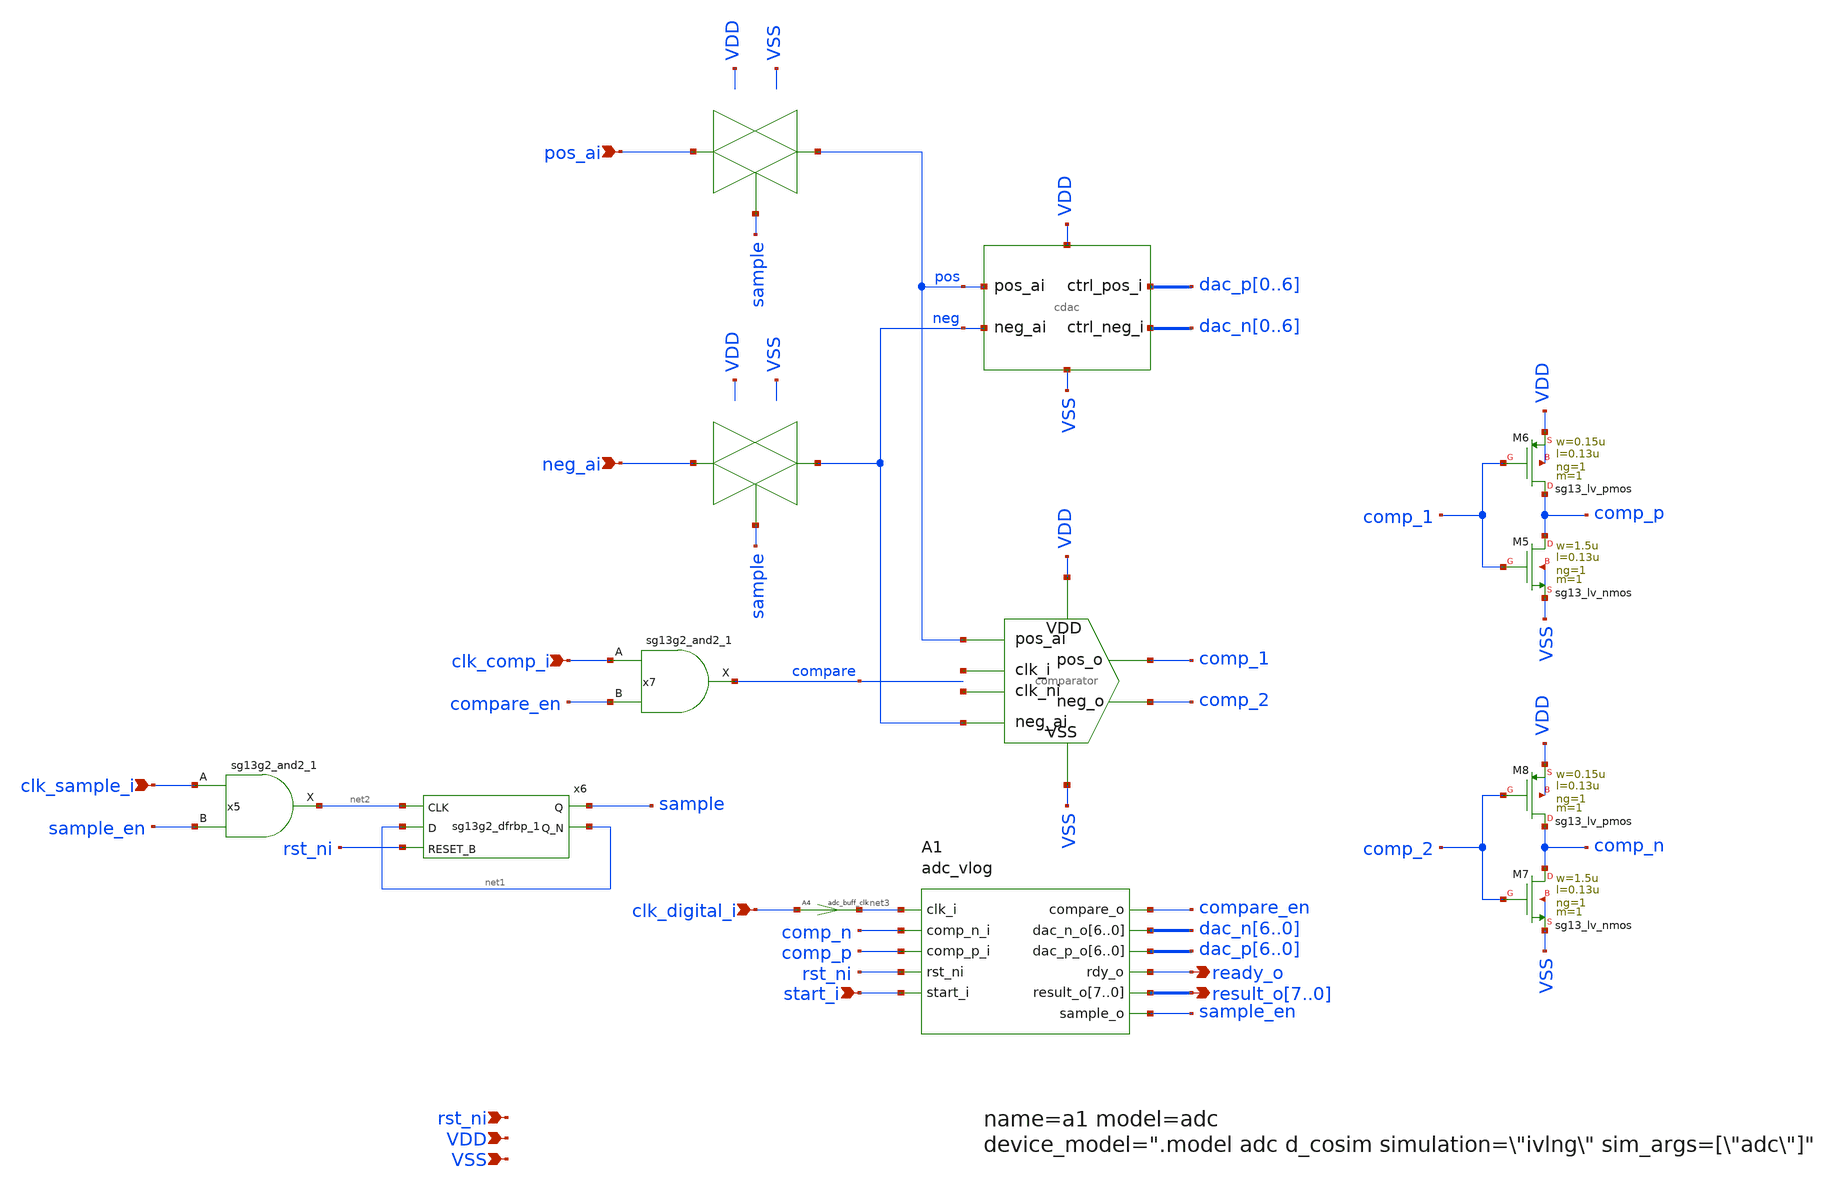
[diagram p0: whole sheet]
** sch_path: project/xschem_gatelevel/adc.sch
* IHP-GmbH/IHP-Open-PDK/ihp-sg13g2/libs.tech/xschem/sg13g2_stdcells/sg13g2_inv_2.sch:
* Copyright 2023 IHP PDK Authors
* Licensed under the Apache License, Version 2.0 (the "License");
**.subckt adc pos_ai VSS VDD clk_comp_i neg_ai clk_sample_i rst_ni clk_digital_i start_i ready_o
*+ result_o7,result_o6,result_o5,result_o4,result_o3,result_o2,result_o1,result_o0
*.ipin pos_ai
*.ipin VSS
*.ipin VDD
*.ipin clk_comp_i
*.ipin neg_ai
*.ipin clk_sample_i
*.ipin rst_ni
*.ipin clk_digital_i
*.ipin start_i
*.opin ready_o
*.opin result_o7,result_o6,result_o5,result_o4,result_o3,result_o2,result_o1,result_o0
x2 net4 pos neg comp_2 comp_1 VSS VDD net5 comparator
x4 pos neg VSS VDD dac_p0 dac_p1 dac_p2 dac_p3 dac_p4 dac_p5 dac_p6 dac_p0 dac_n0 dac_n1 dac_n2
+ dac_n3 dac_n4 dac_n5 dac_n6 dac_n0 cdac
XM5 comp_p comp_1 VSS VSS sg13_lv_nmos w=1.5u l=0.13u ng=1 m=1 mm_ok=1
XM6 comp_p comp_1 VDD VDD sg13_lv_pmos w=0.15u l=0.13u ng=1 m=1 mm_ok=1
XM7 comp_n comp_2 VSS VSS sg13_lv_nmos w=1.5u l=0.13u ng=1 m=1 mm_ok=1
XM8 comp_n comp_2 VDD VDD sg13_lv_pmos w=0.15u l=0.13u ng=1 m=1 mm_ok=1
x6 sample net1 net2 net1 rst_ni VDD VSS sg13g2_dfrbp_1
x5 net2 clk_sample_i sample_en VDD VSS sg13g2_and2_1
x7 compare clk_comp_i compare_en VDD VSS sg13g2_and2_1
A4 [ clk_digital_i ] [ net3 ] adc_buff_clk
A1 [ net3 comp_n comp_p rst_ni start_i ] [ compare_en dac_n6 dac_n5 dac_n4 dac_n3 dac_n2 dac_n1
+ dac_n0 dac_p6 dac_p5 dac_p4 dac_p3 dac_p2 dac_p1 dac_p0 ready_o result_o7 result_o6 result_o5 result_o4
+ result_o3 result_o2 result_o1 result_o0 sample_en ] adc
**.ends

* expanding   symbol:  ./comparator.sym # of pins=8
** sym_path: designs/comparator_dt/comparator.sym
** sch_path: designs/comparator_dt/comparator.sch
.subckt comparator clk_i pos_ai neg_ai neg_o pos_o VSS VDD clk_ni
*.ipin pos_ai
*.ipin neg_ai
*.ipin VSS
*.ipin VDD
*.opin neg_o
*.opin pos_o
*.ipin clk_i
*.ipin clk_ni
XM12 neg_buf clk_i VDD VDD sg13_lv_pmos w=1.0u l=0.13u ng=1 m=1 mm_ok=1
XM13 pos_buf clk_i VDD VDD sg13_lv_pmos w=1.0u l=0.13u ng=1 m=1 mm_ok=1
XM14 net1 pos_ai neg_buf VSS sg13_lv_nmos w=1.0u l=0.13u ng=1 m=1 mm_ok=1
XM15 net1 neg_ai pos_buf VSS sg13_lv_nmos w=1.0u l=0.13u ng=1 m=1 mm_ok=1
XM16 VSS clk_i net1 VSS sg13_lv_nmos w=1.0u l=0.13u ng=1 m=1 mm_ok=1
XM17 net2 clk_ni VDD VDD sg13_lv_pmos w=2.0u l=0.13u ng=2 m=1 mm_ok=1
XM18 pos_o neg_o net2 VDD sg13_lv_pmos w=2.0u l=0.13u ng=2 m=1 mm_ok=1
XM19 neg_o pos_o net2 VDD sg13_lv_pmos w=2.0u l=0.13u ng=2 m=1 mm_ok=1
XM20 VSS neg_buf pos_o VSS sg13_lv_nmos w=1.0u l=0.13u ng=1 m=1 mm_ok=1
XM21 VSS neg_o pos_o VSS sg13_lv_nmos w=1.0u l=0.13u ng=1 m=1 mm_ok=1
XM22 VSS pos_o neg_o VSS sg13_lv_nmos w=1.0u l=0.13u ng=1 m=1 mm_ok=1
XM23 VSS pos_buf neg_o VSS sg13_lv_nmos w=1.0u l=0.13u ng=1 m=1 mm_ok=1
XC1 neg_buf VSS cap_cmim w=1.41e-5 l=1.41e-5 m=1 mm_ok=1
XC2 pos_buf VSS cap_cmim w=1.41e-5 l=1.41e-5 m=1 mm_ok=1
.ends


* expanding   symbol:  ./cdac.sym # of pins=6
** sym_path: designs/cdac_diff/cdac.sym
** sch_path: designs/cdac_diff/cdac.sch
.subckt cdac pos_ai neg_ai VSS VDD pos_ctrl_i0 pos_ctrl_i1 pos_ctrl_i2 pos_ctrl_i3 pos_ctrl_i4
+ pos_ctrl_i5 pos_ctrl_i6 pos_ctrl_i7 neg_ctrl_i0 neg_ctrl_i1 neg_ctrl_i2 neg_ctrl_i3 neg_ctrl_i4 neg_ctrl_i5
+ neg_ctrl_i6 neg_ctrl_i7
*.ipin pos_ai
*.ipin VSS
*.ipin VDD
*.ipin neg_ai
*.ipin
*+ pos_ctrl_i0,pos_ctrl_i1,pos_ctrl_i2,pos_ctrl_i3,pos_ctrl_i4,pos_ctrl_i5,pos_ctrl_i6,pos_ctrl_i7
*.ipin
*+ neg_ctrl_i0,neg_ctrl_i1,neg_ctrl_i2,neg_ctrl_i3,neg_ctrl_i4,neg_ctrl_i5,neg_ctrl_i6,neg_ctrl_i7
x1 net1 pos_ctrl_i0 VDD VSS sg13g2_inv_2
x2 net2 pos_ctrl_i1 VDD VSS sg13g2_inv_2
x3 net3 pos_ctrl_i2 VDD VSS sg13g2_inv_2
x4 net4 pos_ctrl_i3 VDD VSS sg13g2_inv_2
x5 net5 pos_ctrl_i4 VDD VSS sg13g2_inv_2
x6 net6 pos_ctrl_i5 VDD VSS sg13g2_inv_2
x7 net7 pos_ctrl_i6 VDD VSS sg13g2_inv_2
x8 net8 pos_ctrl_i7 VDD VSS sg13g2_inv_2
XC1 pos_ai net8 cap_cmim w=2.5292e-6 l=2.5292e-6 m=1 mm_ok=1
XC2 pos_ai net7 cap_cmim w=2.5292e-6 l=2.5292e-6 m=2 mm_ok=1
XC3 pos_ai net6 cap_cmim w=2.5292e-6 l=2.5292e-6 m=4 mm_ok=1
XC4 pos_ai net5 cap_cmim w=2.5292e-6 l=2.5292e-6 m=8 mm_ok=1
XC9 pos_ai VSS cap_cmim w=2.5292e-6 l=2.5292e-6 m=1 mm_ok=1
x9 net9 neg_ctrl_i0 VDD VSS sg13g2_inv_2
x10 net10 neg_ctrl_i1 VDD VSS sg13g2_inv_2
x11 net11 neg_ctrl_i2 VDD VSS sg13g2_inv_2
x12 net12 neg_ctrl_i3 VDD VSS sg13g2_inv_2
x13 net13 neg_ctrl_i4 VDD VSS sg13g2_inv_2
x14 net14 neg_ctrl_i5 VDD VSS sg13g2_inv_2
x15 net15 neg_ctrl_i6 VDD VSS sg13g2_inv_2
x16 net16 neg_ctrl_i7 VDD VSS sg13g2_inv_2
XC10 neg_ai net16 cap_cmim w=2.5292e-6 l=2.5292e-6 m=1 mm_ok=1
XC11 neg_ai net15 cap_cmim w=2.5292e-6 l=2.5292e-6 m=2 mm_ok=1
XC12 neg_ai net14 cap_cmim w=2.5292e-6 l=2.5292e-6 m=4 mm_ok=1
XC13 neg_ai net13 cap_cmim w=2.5292e-6 l=2.5292e-6 m=8 mm_ok=1
XC18 neg_ai VSS cap_cmim w=2.5292e-6 l=2.5292e-6 m=1 mm_ok=1
XC8 pos_ai net1 cap_cmim w=2.5292e-6 l=2.5292e-6 m=64 mm_ok=1
XC17 neg_ai net9 cap_cmim w=2.5292e-6 l=2.5292e-6 m=64 mm_ok=1
XC19 neg_ai net18 cap_cmim w=2.5292e-6 l=2.5292e-6 m=64 mm_ok=1
XC20 pos_ai net17 cap_cmim w=2.5292e-6 l=2.5292e-6 m=64 mm_ok=1
XC7 neg_ai net10 cap_cmim w=2.5292e-6 l=2.5292e-6 m=32 mm_ok=1
XC16 pos_ai net2 cap_cmim w=2.5292e-6 l=2.5292e-6 m=32 mm_ok=1
XC21 pos_ai net19 cap_cmim w=2.5292e-6 l=2.5292e-6 m=32 mm_ok=1
XC22 neg_ai net20 cap_cmim w=2.5292e-6 l=2.5292e-6 m=32 mm_ok=1
XC23 neg_ai net22 cap_cmim w=2.5292e-6 l=2.5292e-6 m=16 mm_ok=1
XC24 pos_ai net21 cap_cmim w=2.5292e-6 l=2.5292e-6 m=16 mm_ok=1
XC6 neg_ai net11 cap_cmim w=2.5292e-6 l=2.5292e-6 m=16 mm_ok=1
XC15 pos_ai net3 cap_cmim w=2.5292e-6 l=2.5292e-6 m=16 mm_ok=1
XC25 neg_ai net24 cap_cmim w=2.5292e-6 l=2.5292e-6 m=8 mm_ok=1
XC26 pos_ai net23 cap_cmim w=2.5292e-6 l=2.5292e-6 m=8 mm_ok=1
XC5 pos_ai net4 cap_cmim w=2.5292e-6 l=2.5292e-6 m=8 mm_ok=1
XC14 neg_ai net12 cap_cmim w=2.5292e-6 l=2.5292e-6 m=8 mm_ok=1
* noconn VDD
x17 net17 neg_ctrl_i0 VDD VSS sg13g2_buf_2
x21 net18 pos_ctrl_i0 VDD VSS sg13g2_buf_2
x18 net19 neg_ctrl_i1 VDD VSS sg13g2_buf_2
x19 net20 pos_ctrl_i1 VDD VSS sg13g2_buf_2
x20 net21 neg_ctrl_i2 VDD VSS sg13g2_buf_2
x22 net22 pos_ctrl_i2 VDD VSS sg13g2_buf_2
x23 net23 neg_ctrl_i3 VDD VSS sg13g2_buf_2
x24 net24 pos_ctrl_i3 VDD VSS sg13g2_buf_2
.ends


* expanding   symbol:  sg13g2_stdcells/sg13g2_dfrbp_1.sym # of pins=5
** sym_path: sg13g2_stdcells/sg13g2_dfrbp_1.sym
** sch_path: sg13g2_stdcells/sg13g2_dfrbp_1.sch
.subckt sg13g2_dfrbp_1 Q Q_N CLK D RESET_B VDD VSS
*.ipin D
*.ipin RESET_B
*.ipin CLK
*.opin Q
*.opin Q_N
*.iopin VDD
*.iopin VSS
XM1 Db D net10 VSS sg13_lv_nmos w=420.00n l=130.00n ng=1 m=1 mm_ok=1
XM2 net10 RESET_B VSS VSS sg13_lv_nmos w=420.00n l=130.00n ng=1 m=1 mm_ok=1
XM3 net1 clkneg net9 VSS sg13_lv_nmos w=420.00n l=130.00n ng=1 m=1 mm_ok=1
XM4 net9 net1 VSS VSS sg13_lv_nmos w=420.00n l=130.00n ng=1 m=1 mm_ok=1
XM5 net1 net1 net5 VSS sg13_lv_nmos w=420.00n l=130.00n ng=1 m=1 mm_ok=1
XM6 net5 RESET_B VSS VSS sg13_lv_nmos w=420.00n l=130.00n ng=1 m=1 mm_ok=1
XM7 Q_N net1 VSS VSS sg13_lv_nmos w=740.00n l=130.00n ng=1 m=1 mm_ok=1
XM8 net2 net1 VSS VSS sg13_lv_nmos w=740.00n l=130.00n ng=1 m=1 mm_ok=1
XM9 Q net2 VSS VSS sg13_lv_nmos w=740.00n l=130.00n ng=1 m=1 mm_ok=1
XM10 clkneg CLK VSS VSS sg13_lv_nmos w=740.00n l=130.00n ng=1 m=1 mm_ok=1
XM11 clkpos clkneg VSS VSS sg13_lv_nmos w=740.00n l=130.00n ng=1 m=1 mm_ok=1
XM12 Db clkneg net3 VSS sg13_lv_nmos w=420.00n l=130.00n ng=1 m=1 mm_ok=1
XM13 net3 clkpos net8 VSS sg13_lv_nmos w=420.00n l=130.00n ng=1 m=1 mm_ok=1
XM14 net8 net3 net4 VSS sg13_lv_nmos w=420.00n l=130.00n ng=1 m=1 mm_ok=1
XM15 net4 RESET_B VSS VSS sg13_lv_nmos w=420.00n l=130.00n ng=1 m=1 mm_ok=1
XM16 net3 net3 VSS VSS sg13_lv_nmos w=740.00n l=130.00n ng=1 m=1 mm_ok=1
XM17 net3 clkpos net1 VSS sg13_lv_nmos w=740.00n l=130.00n ng=1 m=1 mm_ok=1
XM18 Db RESET_B VDD VDD sg13_lv_pmos w=420.00n l=130.00n ng=1 m=1 mm_ok=1
XM19 Db D VDD VDD sg13_lv_pmos w=420.00n l=130.00n ng=1 m=1 mm_ok=1
XM20 net7 net1 VDD VDD sg13_lv_pmos w=420.00n l=130.00n ng=1 m=1 mm_ok=1
XM21 net1 clkpos net7 VDD sg13_lv_pmos w=420.00n l=130.00n ng=1 m=1 mm_ok=1
XM22 net1 net1 VDD VDD sg13_lv_pmos w=420.00n l=130.00n ng=1 m=1 mm_ok=1
XM23 net1 RESET_B VDD VDD sg13_lv_pmos w=420.00n l=130.00n ng=1 m=1 mm_ok=1
XM24 Q_N net1 VDD VDD sg13_lv_pmos w=1.12u l=130.00n ng=1 m=1 mm_ok=1
XM25 net2 net1 VDD VDD sg13_lv_pmos w=1.12u l=130.00n ng=1 m=1 mm_ok=1
XM26 Q net2 VDD VDD sg13_lv_pmos w=1.12u l=130.00n ng=1 m=1 mm_ok=1
XM27 clkneg CLK VDD VDD sg13_lv_pmos w=1.12u l=130.00n ng=1 m=1 mm_ok=1
XM28 clkpos clkneg VDD VDD sg13_lv_pmos w=1.12u l=130.00n ng=1 m=1 mm_ok=1
XM29 Db clkpos net3 VDD sg13_lv_pmos w=420.00n l=130.00n ng=1 m=1 mm_ok=1
XM30 net6 net3 VDD VDD sg13_lv_pmos w=420.00n l=130.00n ng=1 m=1 mm_ok=1
XM31 net3 clkneg net6 VDD sg13_lv_pmos w=420.00n l=130.00n ng=1 m=1 mm_ok=1
XM32 net3 RESET_B VDD VDD sg13_lv_pmos w=420.00n l=130.00n ng=1 m=1 mm_ok=1
XM33 net3 net3 VDD VDD sg13_lv_pmos w=1.000u l=130.00n ng=1 m=1 mm_ok=1
XM34 net3 clkneg net1 VDD sg13_lv_pmos w=1.000u l=130.00n ng=1 m=1 mm_ok=1
.ends


* expanding   symbol:  sg13g2_stdcells/sg13g2_and2_1.sym # of pins=3
** sym_path: sg13g2_stdcells/sg13g2_and2_1.sym
** sch_path: sg13g2_stdcells/sg13g2_and2_1.sch
.subckt sg13g2_and2_1 X A B VDD VSS
*.ipin A
*.ipin B
*.opin X
*.iopin VDD
*.iopin VSS
XM1 net1 A net2 VSS sg13_lv_nmos w=640.00n l=130.00n ng=1 m=1 mm_ok=1
XM2 net2 B VSS VSS sg13_lv_nmos w=640.00n l=130.00n ng=1 m=1 mm_ok=1
XM3 X net1 VSS VSS sg13_lv_nmos w=740.00n l=130.00n ng=1 m=1 mm_ok=1
XM4 net1 B VDD VDD sg13_lv_pmos w=840.00n l=130.00n ng=1 m=1 mm_ok=1
XM5 net1 A VDD VDD sg13_lv_pmos w=840.00n l=130.00n ng=1 m=1 mm_ok=1
XM6 X net1 VDD VDD sg13_lv_pmos w=1.12u l=130.00n ng=1 m=1 mm_ok=1
.ends


* expanding   symbol:  sg13g2_stdcells/sg13g2_inv_2.sym # of pins=2
** sym_path: sg13g2_stdcells/sg13g2_inv_2.sym
** sch_path: sg13g2_stdcells/sg13g2_inv_2.sch
.subckt sg13g2_inv_2 Y A VDD VSS
*.opin Y
*.ipin A
*.iopin VDD
*.iopin VSS
XM1 Y A VSS VSS sg13_lv_nmos w=1.48u l=130.00n ng=2 m=1 mm_ok=1
XM2 Y A VDD VDD sg13_lv_pmos w=2.24u l=130.00n ng=2 m=1 mm_ok=1
.ends


* expanding   symbol:  sg13g2_stdcells/sg13g2_buf_2.sym # of pins=2
** sym_path: sg13g2_stdcells/sg13g2_buf_2.sym
** sch_path: sg13g2_stdcells/sg13g2_buf_2.sch
.subckt sg13g2_buf_2 X A VDD VSS
*.ipin A
*.opin X
*.iopin VDD
*.iopin VSS
XM1 net1 A VSS VSS sg13_lv_nmos w=640.00n l=130.00n ng=1 m=1 mm_ok=1
XM2 X net1 VSS VSS sg13_lv_nmos w=1.48u l=130.00n ng=2 m=1 mm_ok=1
XM3 net1 A VDD VDD sg13_lv_pmos w=1.000u l=130.00n ng=1 m=1 mm_ok=1
XM4 X net1 VDD VDD sg13_lv_pmos w=2.24u l=130.00n ng=2 m=1 mm_ok=1
.ends

**** begin user architecture code
.model adc d_cosim simulation="ivlng" sim_args=["adc"]
**** end user architecture code
.end
